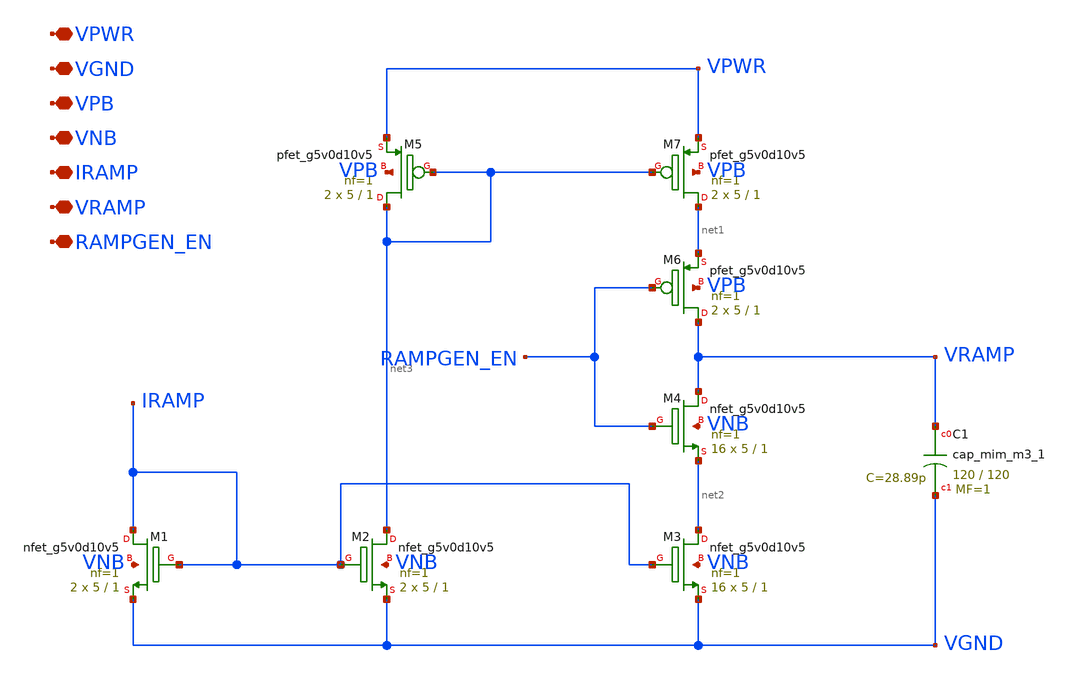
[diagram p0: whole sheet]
** sch_path: design/oscillator/rampgen.sch
**.subckt rampgen VPWR VGND VPB VNB IRAMP VRAMP RAMPGEN_EN
*.iopin VPWR
*.iopin VGND
*.iopin VPB
*.iopin VNB
*.iopin IRAMP
*.iopin VRAMP
*.iopin RAMPGEN_EN
XM1 IRAMP IRAMP VGND VNB sky130_fd_pr__nfet_g5v0d10v5 L=1 W=5 nf=1 ad='int((nf+1)/2) * W/nf * 0.29' as='int((nf+2)/2) * W/nf * 0.29'
+ pd='2*int((nf+1)/2) * (W/nf + 0.29)' ps='2*int((nf+2)/2) * (W/nf + 0.29)' nrd='0.29 / W' nrs='0.29 / W'
+ sa=0 sb=0 sd=0 mult=2 m=2
XM2 net3 IRAMP VGND VNB sky130_fd_pr__nfet_g5v0d10v5 L=1 W=5 nf=1 ad='int((nf+1)/2) * W/nf * 0.29' as='int((nf+2)/2) * W/nf * 0.29'
+ pd='2*int((nf+1)/2) * (W/nf + 0.29)' ps='2*int((nf+2)/2) * (W/nf + 0.29)' nrd='0.29 / W' nrs='0.29 / W'
+ sa=0 sb=0 sd=0 mult=2 m=2
XM3 net2 IRAMP VGND VNB sky130_fd_pr__nfet_g5v0d10v5 L=1 W=5 nf=1 ad='int((nf+1)/2) * W/nf * 0.29' as='int((nf+2)/2) * W/nf * 0.29'
+ pd='2*int((nf+1)/2) * (W/nf + 0.29)' ps='2*int((nf+2)/2) * (W/nf + 0.29)' nrd='0.29 / W' nrs='0.29 / W'
+ sa=0 sb=0 sd=0 mult=16 m=16
XM4 VRAMP RAMPGEN_EN net2 VNB sky130_fd_pr__nfet_g5v0d10v5 L=1 W=5 nf=1 ad='int((nf+1)/2) * W/nf * 0.29'
+ as='int((nf+2)/2) * W/nf * 0.29' pd='2*int((nf+1)/2) * (W/nf + 0.29)' ps='2*int((nf+2)/2) * (W/nf + 0.29)'
+ nrd='0.29 / W' nrs='0.29 / W' sa=0 sb=0 sd=0 mult=16 m=16
XM5 net3 net3 VPWR VPB sky130_fd_pr__pfet_g5v0d10v5 L=1 W=5 nf=1 ad='int((nf+1)/2) * W/nf * 0.29' as='int((nf+2)/2) * W/nf * 0.29'
+ pd='2*int((nf+1)/2) * (W/nf + 0.29)' ps='2*int((nf+2)/2) * (W/nf + 0.29)' nrd='0.29 / W' nrs='0.29 / W'
+ sa=0 sb=0 sd=0 mult=2 m=2
XM6 VRAMP RAMPGEN_EN net1 VPB sky130_fd_pr__pfet_g5v0d10v5 L=1 W=5 nf=1 ad='int((nf+1)/2) * W/nf * 0.29'
+ as='int((nf+2)/2) * W/nf * 0.29' pd='2*int((nf+1)/2) * (W/nf + 0.29)' ps='2*int((nf+2)/2) * (W/nf + 0.29)'
+ nrd='0.29 / W' nrs='0.29 / W' sa=0 sb=0 sd=0 mult=2 m=2
XM7 net1 net3 VPWR VPB sky130_fd_pr__pfet_g5v0d10v5 L=1 W=5 nf=1 ad='int((nf+1)/2) * W/nf * 0.29' as='int((nf+2)/2) * W/nf * 0.29'
+ pd='2*int((nf+1)/2) * (W/nf + 0.29)' ps='2*int((nf+2)/2) * (W/nf + 0.29)' nrd='0.29 / W' nrs='0.29 / W'
+ sa=0 sb=0 sd=0 mult=2 m=2
XC1 VRAMP VGND sky130_fd_pr__cap_mim_m3_1 W=120 L=120 MF=1 m=1
**.ends
.end
